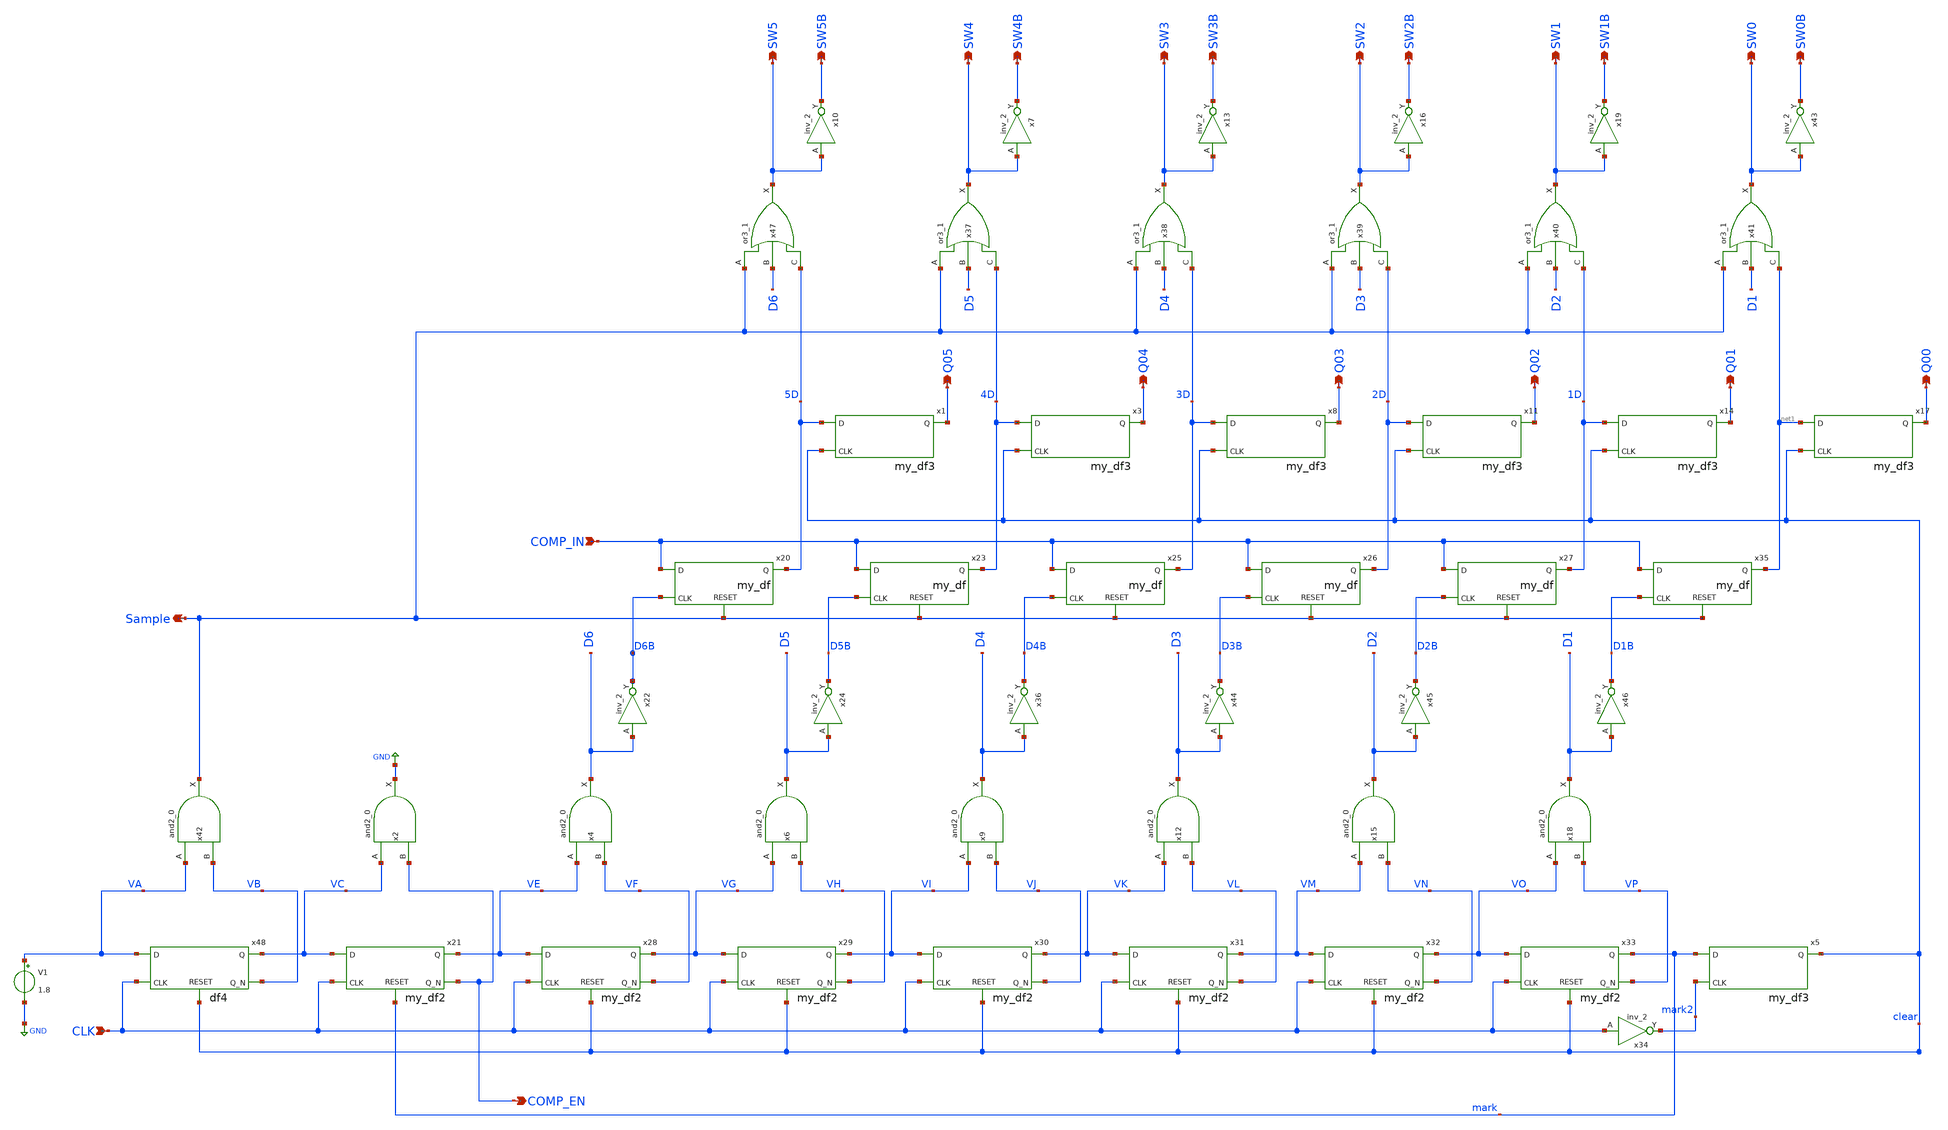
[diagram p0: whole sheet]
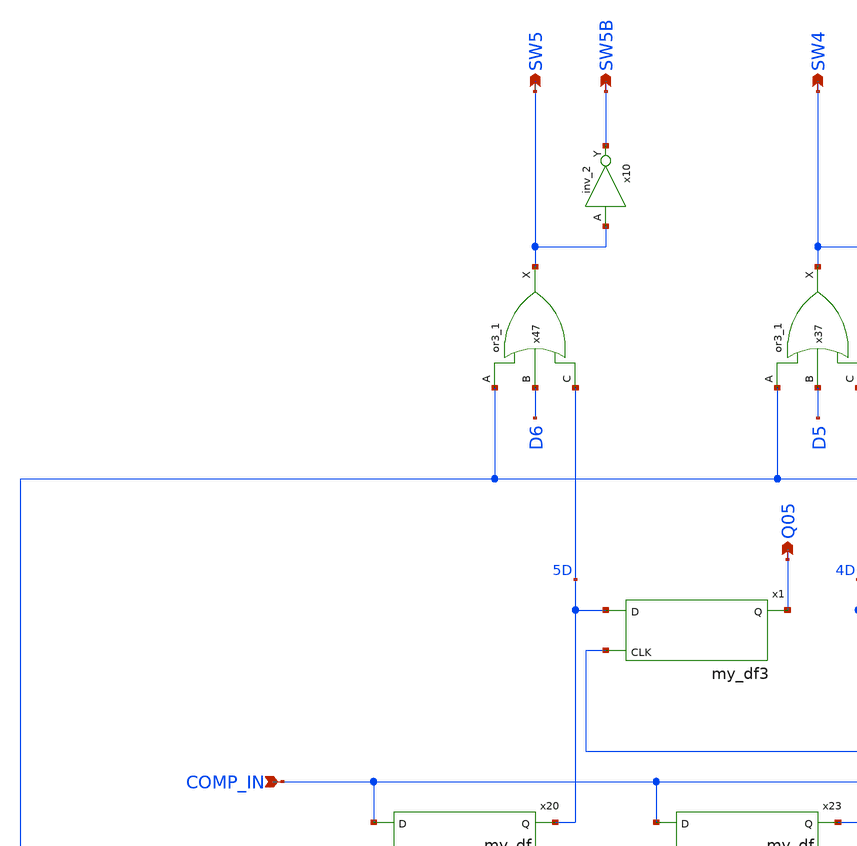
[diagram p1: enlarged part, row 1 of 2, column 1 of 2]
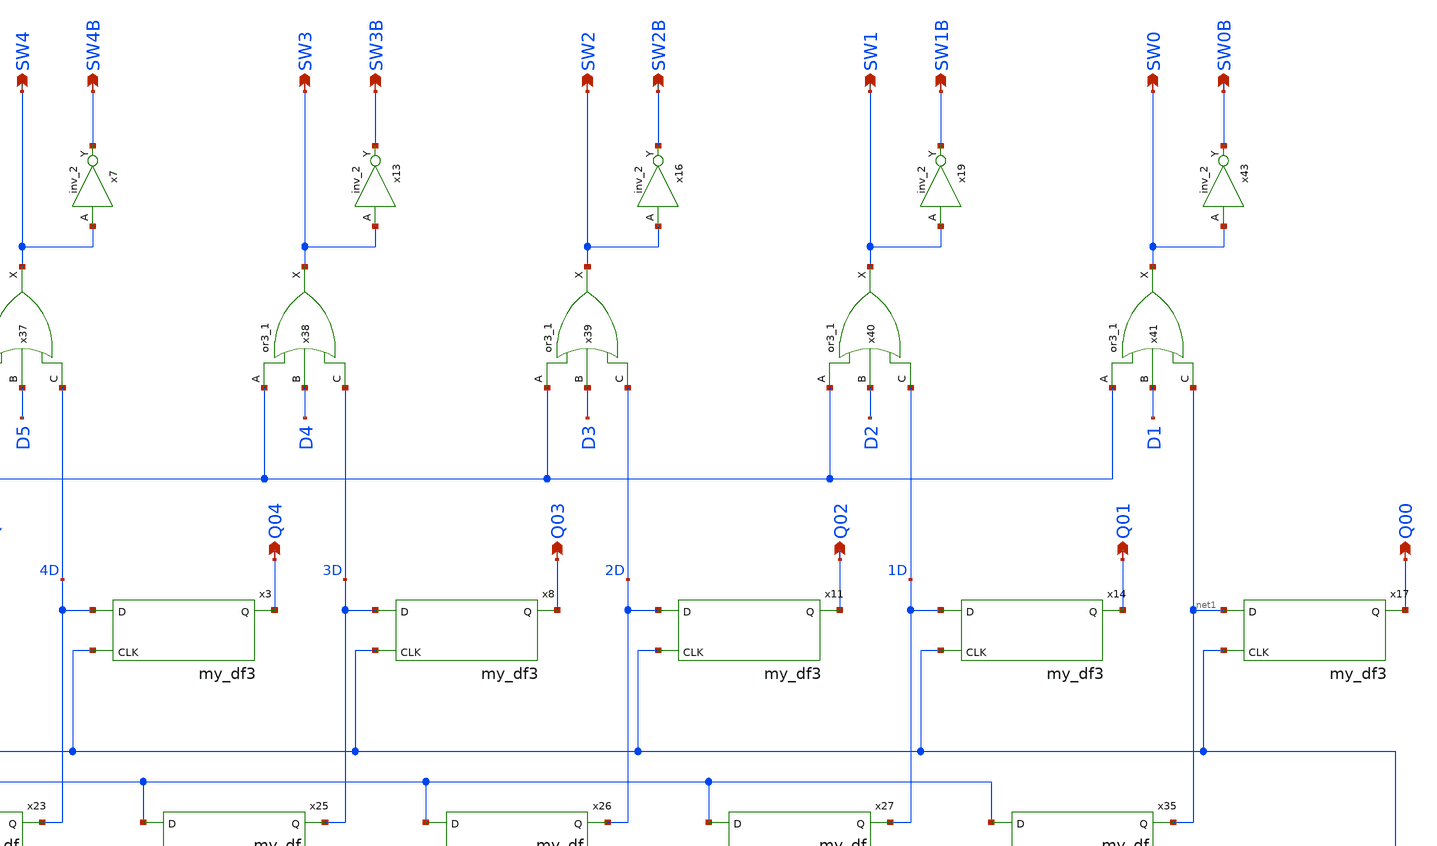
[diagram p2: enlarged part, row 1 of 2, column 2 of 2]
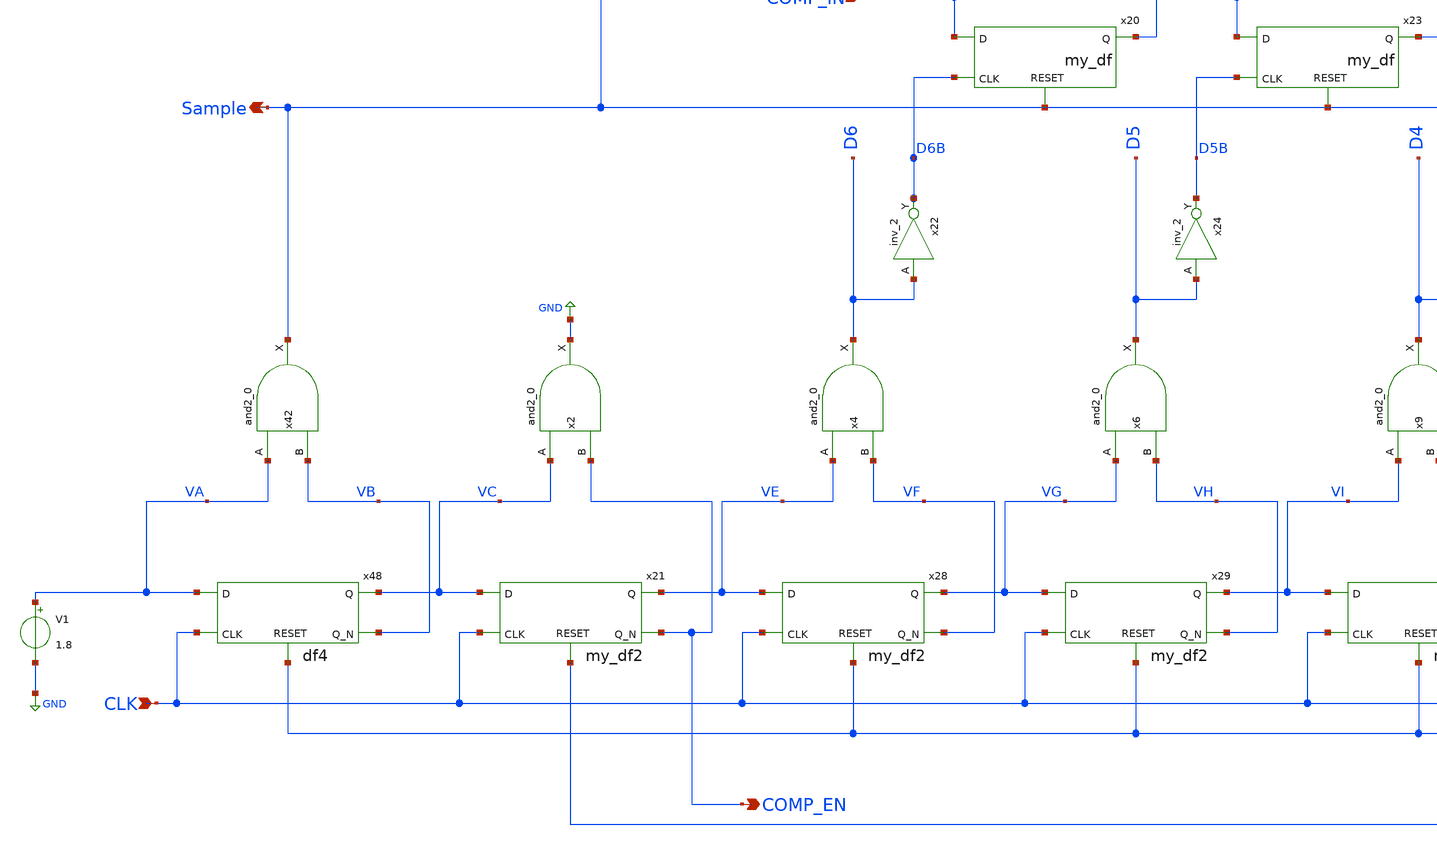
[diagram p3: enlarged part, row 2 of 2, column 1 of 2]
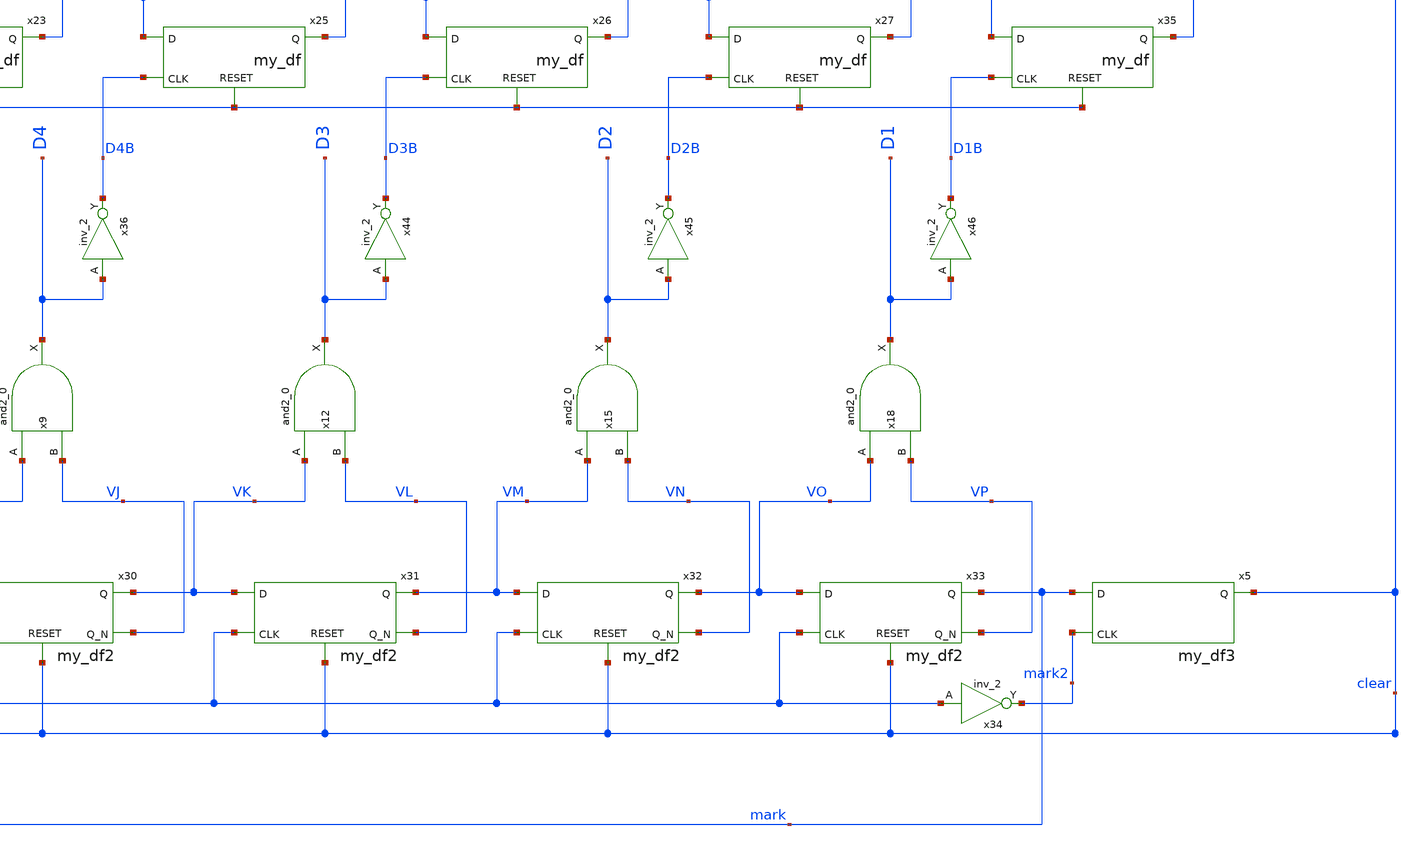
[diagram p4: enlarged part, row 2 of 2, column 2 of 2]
** sch_path: xschem/my_sar_logic.sch
**.subckt my_sar_logic Sample COMP_IN Q05 Q04 Q03 Q02 Q01 Q00 SW5 SW4 SW4B SW3 SW3B SW2 SW2B SW1
*+ SW1B SW0 SW0B SW5B CLK COMP_EN
*.opin Sample
*.ipin COMP_IN
*.opin Q05
*.opin Q04
*.opin Q03
*.opin Q02
*.opin Q01
*.opin Q00
*.opin SW5
*.opin SW4
*.opin SW4B
*.opin SW3
*.opin SW3B
*.opin SW2
*.opin SW2B
*.opin SW1
*.opin SW1B
*.opin SW0
*.opin SW0B
*.opin SW5B
*.ipin CLK
*.opin COMP_EN
x7 SW4 GND GND VDD VDD SW4B sky130_fd_sc_hd__inv_2
x10 SW5 GND GND VDD VDD SW5B sky130_fd_sc_hd__inv_2
x13 SW3 GND GND VDD VDD SW3B sky130_fd_sc_hd__inv_2
x16 SW2 GND GND VDD VDD SW2B sky130_fd_sc_hd__inv_2
x19 SW1 GND GND VDD VDD SW1B sky130_fd_sc_hd__inv_2
x43 SW0 GND GND VDD VDD SW0B sky130_fd_sc_hd__inv_2
x47 Sample D6 5D GND GND VDD VDD SW5 sky130_fd_sc_hd__or3_1
x37 Sample D5 4D GND GND VDD VDD SW4 sky130_fd_sc_hd__or3_1
x38 Sample D4 3D GND GND VDD VDD SW3 sky130_fd_sc_hd__or3_1
x39 Sample D3 2D GND GND VDD VDD SW2 sky130_fd_sc_hd__or3_1
x40 Sample D2 1D GND GND VDD VDD SW1 sky130_fd_sc_hd__or3_1
x41 Sample D1 net1 GND GND VDD VDD SW0 sky130_fd_sc_hd__or3_1
x20 D6B 5D COMP_IN Sample my_df
x23 D5B 4D COMP_IN Sample my_df
x25 D4B 3D COMP_IN Sample my_df
x26 D3B 2D COMP_IN Sample my_df
x27 D2B 1D COMP_IN Sample my_df
x35 D1B net1 COMP_IN Sample my_df
V1 VA GND 1.8
x22 D6 GND GND VDD VDD D6B sky130_fd_sc_hd__inv_2
x24 D5 GND GND VDD VDD D5B sky130_fd_sc_hd__inv_2
x36 D4 GND GND VDD VDD D4B sky130_fd_sc_hd__inv_2
x44 D3 GND GND VDD VDD D3B sky130_fd_sc_hd__inv_2
x45 D2 GND GND VDD VDD D2B sky130_fd_sc_hd__inv_2
x46 D1 GND GND VDD VDD D1B sky130_fd_sc_hd__inv_2
x42 VA VB GND GND VDD VDD Sample sky130_fd_sc_hd__and2_0
x2 VC COMP_EN GND GND VDD VDD GND sky130_fd_sc_hd__and2_0
x4 VE VF GND GND VDD VDD D6 sky130_fd_sc_hd__and2_0
x6 VG VH GND GND VDD VDD D5 sky130_fd_sc_hd__and2_0
x9 VI VJ GND GND VDD VDD D4 sky130_fd_sc_hd__and2_0
x12 VK VL GND GND VDD VDD D3 sky130_fd_sc_hd__and2_0
x15 VM VN GND GND VDD VDD D2 sky130_fd_sc_hd__and2_0
x18 VO VP GND GND VDD VDD D1 sky130_fd_sc_hd__and2_0
x21 CLK VE VC COMP_EN mark my_df2
x28 CLK VG VE VF clear my_df2
x29 CLK VI VG VH clear my_df2
x30 CLK VK VI VJ clear my_df2
x31 CLK VM VK VL clear my_df2
x32 CLK VO VM VN clear my_df2
x33 CLK mark VO VP clear my_df2
x34 CLK GND GND VDD VDD mark2 sky130_fd_sc_hd__inv_2
x5 mark2 clear mark my_df3
x48 CLK VC VA VB clear df4
x1 clear Q05 5D my_df3
x3 clear Q04 4D my_df3
x8 clear Q03 3D my_df3
x11 clear Q02 2D my_df3
x14 clear Q01 1D my_df3
x17 clear Q00 net1 my_df3
**.ends

* expanding   symbol:  my_df.sym # of pins=4
** sym_path: xschem/my_df.sym
** sch_path: xschem/my_df.sch
.subckt my_df CLK Q D RESET
*.ipin CLK
*.ipin D
*.ipin RESET
*.opin Q
x1 RESET GND GND VDD VDD net1 sky130_fd_sc_hd__inv_1
x3 CLK D net1 GND GND VDD VDD Q sky130_fd_sc_hd__dfrtp_1
.ends


* expanding   symbol:  my_df2.sym # of pins=5
** sym_path: xschem/my_df2.sym
** sch_path: xschem/my_df2.sch
.subckt my_df2 CLK Q D Q_N RESET
*.ipin CLK
*.ipin D
*.ipin RESET
*.opin Q
*.opin Q_N
x1 RESET GND GND VDD VDD net1 sky130_fd_sc_hd__inv_1
x2 CLK D net1 VDD GND GND VDD VDD Q Q_N sky130_fd_sc_hd__dfbbp_1
.ends


* expanding   symbol:  my_df3.sym # of pins=3
** sym_path: xschem/my_df3.sym
** sch_path: xschem/my_df3.sch
.subckt my_df3 CLK Q D
*.ipin CLK
*.ipin D
*.opin Q
x1 CLK D VDD GND GND VDD VDD Q sky130_fd_sc_hd__dfrtp_1
.ends


* expanding   symbol:  df4.sym # of pins=5
** sym_path: xschem/df4.sym
** sch_path: xschem/df4.sch
.subckt df4 CLK Q D Q_N RESET
*.ipin CLK
*.ipin D
*.ipin RESET
*.opin Q
*.opin Q_N
x2 RESET GND GND VDD VDD net1 sky130_fd_sc_hd__inv_1
x1 CLK D net1 GND GND VDD VDD Q Q_N sky130_fd_sc_hd__dfrbp_1
.ends

.GLOBAL GND
.GLOBAL VDD
.end
